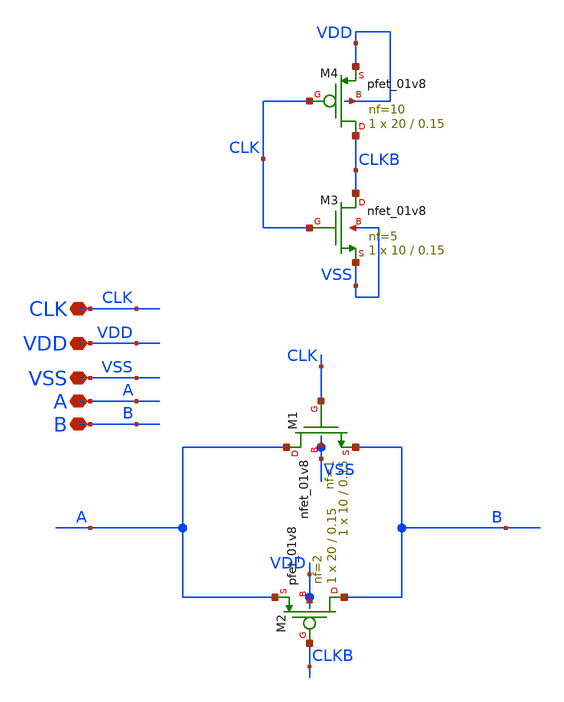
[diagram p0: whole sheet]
** sch_path: xschem/xschem_BGR_Top/Sigma_Delta/Transmission_Gate/TG.sch
**.subckt TG VDD VSS A B CLK
*.iopin VDD
*.iopin VSS
*.iopin A
*.iopin B
*.iopin CLK
XM1 A CLK B VSS sky130_fd_pr__nfet_01v8 L=0.15 W=10 nf=1 ad='int((nf+1)/2) * W/nf * 0.29' as='int((nf+2)/2) * W/nf * 0.29'
+ pd='2*int((nf+1)/2) * (W/nf + 0.29)' ps='2*int((nf+2)/2) * (W/nf + 0.29)' nrd='0.29 / W' nrs='0.29 / W'
+ sa=0 sb=0 sd=0 mult=1 m=1
XM2 B CLKB A VDD sky130_fd_pr__pfet_01v8 L=0.15 W=20 nf=2 ad='int((nf+1)/2) * W/nf * 0.29' as='int((nf+2)/2) * W/nf * 0.29'
+ pd='2*int((nf+1)/2) * (W/nf + 0.29)' ps='2*int((nf+2)/2) * (W/nf + 0.29)' nrd='0.29 / W' nrs='0.29 / W'
+ sa=0 sb=0 sd=0 mult=1 m=1
XM3 CLKB CLK VSS VSS sky130_fd_pr__nfet_01v8 L=0.15 W=10 nf=5 ad='int((nf+1)/2) * W/nf * 0.29' as='int((nf+2)/2) * W/nf * 0.29'
+ pd='2*int((nf+1)/2) * (W/nf + 0.29)' ps='2*int((nf+2)/2) * (W/nf + 0.29)' nrd='0.29 / W' nrs='0.29 / W'
+ sa=0 sb=0 sd=0 mult=1 m=1
XM4 CLKB CLK VDD VDD sky130_fd_pr__pfet_01v8 L=0.15 W=20 nf=10 ad='int((nf+1)/2) * W/nf * 0.29' as='int((nf+2)/2) * W/nf * 0.29'
+ pd='2*int((nf+1)/2) * (W/nf + 0.29)' ps='2*int((nf+2)/2) * (W/nf + 0.29)' nrd='0.29 / W' nrs='0.29 / W'
+ sa=0 sb=0 sd=0 mult=1 m=1
**.ends
.end
